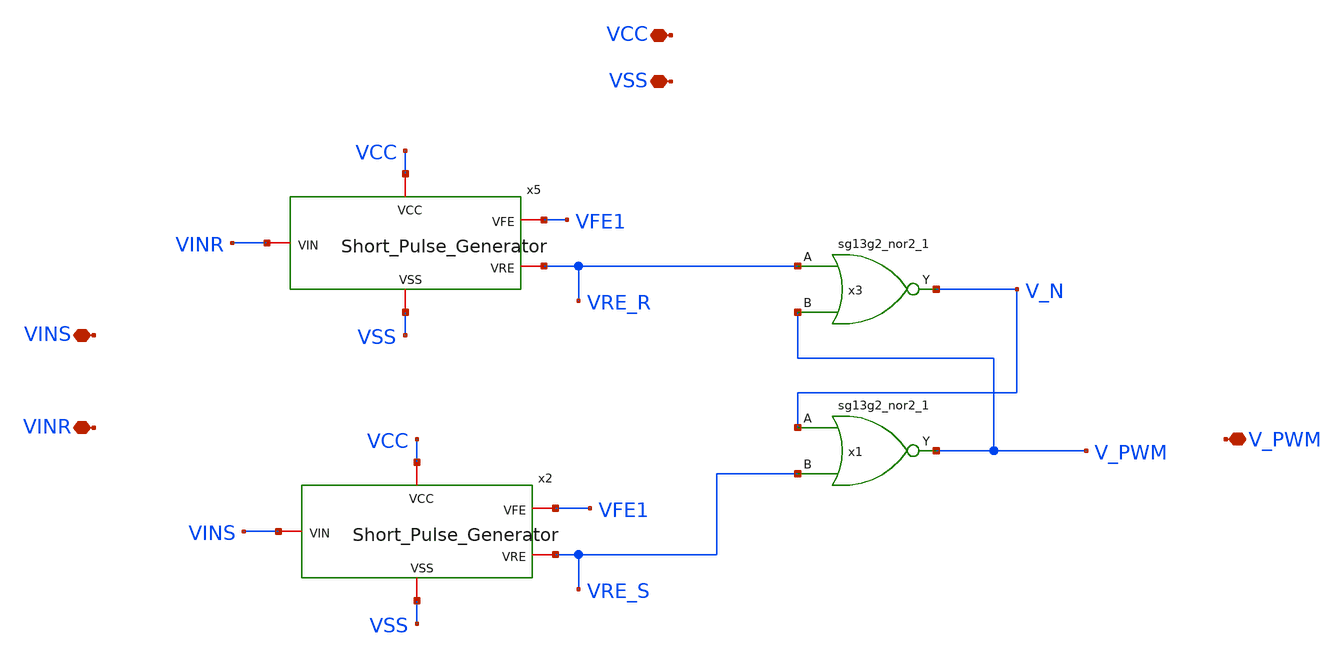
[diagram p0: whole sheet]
** sch_path: ChipUSM_AnalogTrack24/PD/PhaseDetector.sch
**.subckt PhaseDetector V_PWM VCC VSS VINS VINR
*.iopin V_PWM
*.iopin VCC
*.iopin VSS
*.iopin VINS
*.iopin VINR
x3 V_N VRE_R V_PWM VCC VSS sg13g2_nor2_1
x1 V_PWM V_N VRE_S VCC VSS sg13g2_nor2_1
x5 VCC VSS VFE1 VINR VRE_R Short_Pulse_Generator
x2 VCC VSS VFE1 VINS VRE_S Short_Pulse_Generator
**.ends
.end
